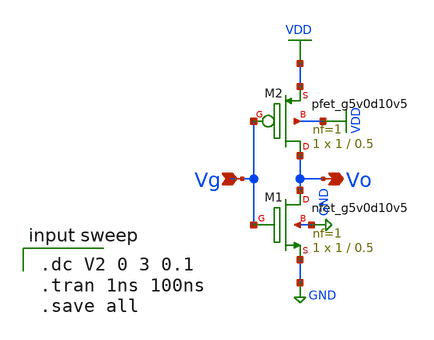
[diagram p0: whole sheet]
** sch_path: SMPS_Without_Deadtime/inverter.sch
**.subckt inverter Vo Vg
*.opin Vo
*.ipin Vg
XM2 Vo Vg VDD VDD sky130_fd_pr__pfet_g5v0d10v5 L=0.5 W=1 nf=1 ad='int((nf+1)/2) * W/nf * 0.29' as='int((nf+2)/2) * W/nf * 0.29'
+ pd='2*int((nf+1)/2) * (W/nf + 0.29)' ps='2*int((nf+2)/2) * (W/nf + 0.29)' nrd='0.29 / W' nrs='0.29 / W'
+ sa=0 sb=0 sd=0 mult=1 m=1
XM1 Vo Vg GND GND sky130_fd_pr__nfet_g5v0d10v5 L=0.5 W=1 nf=1 ad='int((nf+1)/2) * W/nf * 0.29' as='int((nf+2)/2) * W/nf * 0.29'
+ pd='2*int((nf+1)/2) * (W/nf + 0.29)' ps='2*int((nf+2)/2) * (W/nf + 0.29)' nrd='0.29 / W' nrs='0.29 / W'
+ sa=0 sb=0 sd=0 mult=1 m=1
**** begin user architecture code
 .lib $::SKYWATER_MODELS/sky130.lib.spice tt

.dc V2 0 3 0.1
.tran 1ns 100ns
.save all

**** end user architecture code
**.ends
.GLOBAL VDD
.GLOBAL GND
.end
